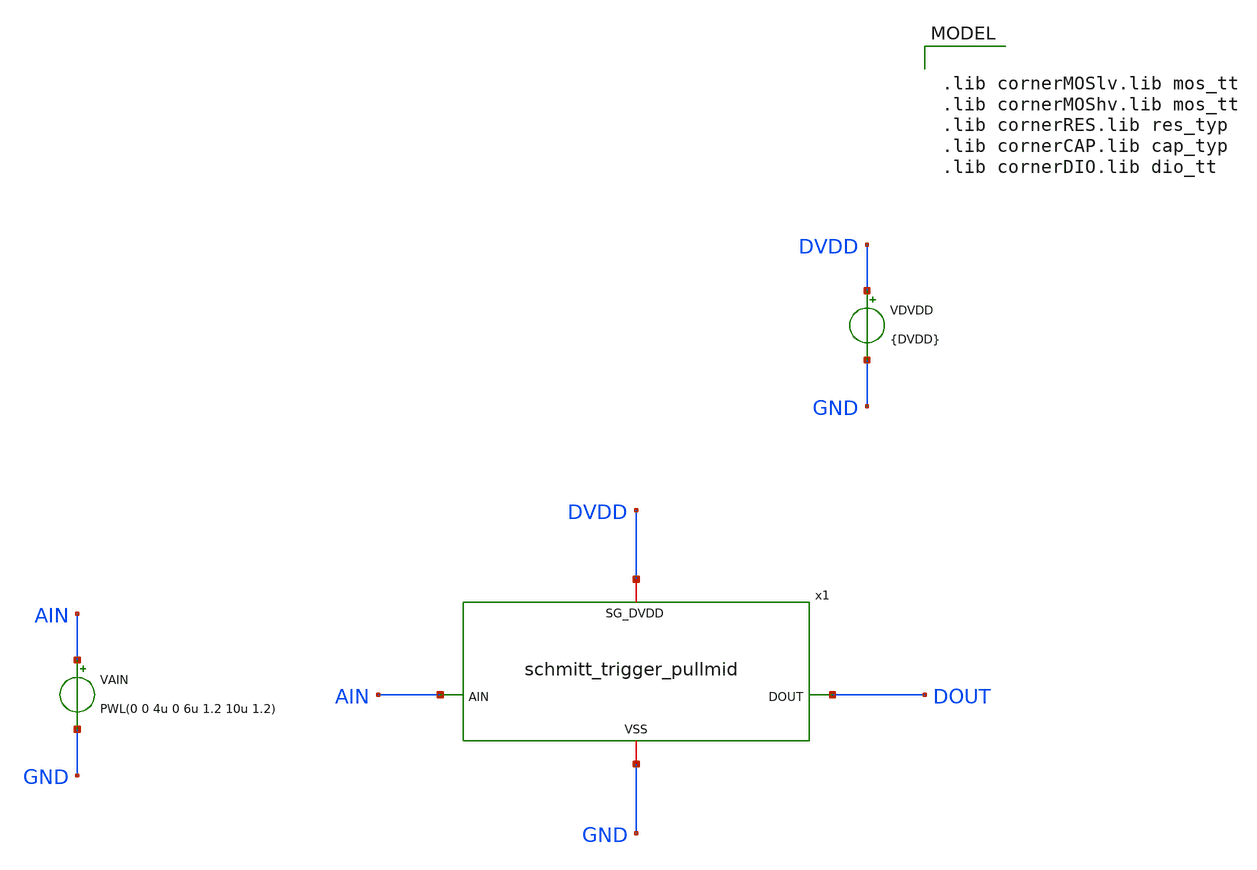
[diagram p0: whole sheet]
** sch_path: macros/schmitt_trigger_pullmid/testbenches/xschem/schmitt_trigger_pullmid_tb_dc.sch
**.subckt schmitt_trigger_pullmid_tb_dc
x1 DVDD AIN DOUT GND schmitt_trigger_pullmid
VAIN AIN GND PWL(0 0 4u 0 6u 1.2 10u 1.2)
VDVDD DVDD GND {DVDD}
**** begin user architecture code


.include ../../../netlist/pex/schmitt_trigger_pullmid_magic_pex_3.spice
.param DVDD=1.2
.csparam DVDD=DVDD
.temp 27
.options savecurrents klu method=gear reltol=1e-3 abstol=1e-12 gmin=1e-12
.control

save all

tran 100p 10u
write @schname\.raw

plot ain dout

unset appendwrite
set wr_vecnames
set wr_singlescale
wrdata ../plot_simulations/data/@schname\.txt v(ain) v(dout)

*quit
.endc



.lib cornerMOSlv.lib mos_tt
.lib cornerMOShv.lib mos_tt
.lib cornerRES.lib res_typ
.lib cornerCAP.lib cap_typ
.lib cornerDIO.lib dio_tt

**** end user architecture code
**.ends

* expanding   symbol:  schmitt_trigger_pullmid.sym # of pins=4
** sym_path: schmitt_trigger_pullmid.sym
** sch_path: schmitt_trigger_pullmid.sch
.subckt schmitt_trigger_pullmid SG_DVDD AIN DOUT VSS
*.iopin SG_DVDD
*.iopin VSS
*.ipin AIN
*.opin DOUT
Vmeas6 AIN net1 0
.save i(vmeas6)
XR1 SG_DVDD MID VSS rhigh w=0.5e-6 l=3.412e-05 m=1 b=0 mm_ok=1
XR2 MID VSS VSS rhigh w=0.5e-6 l=3.412e-05 m=1 b=0 mm_ok=1
XR3 net1 MID VSS rhigh w=0.5e-6 l=2.7172e-04 m=1 b=0 mm_ok=1
XC4 VSS SG_DVDD cap_cmomf w=30.0e-6 l=75.0e-6 mmin=1 mmax=4 subblock=0 rfmodel=0 subscale=1 m=1
+ mm_ok=1
XM4 DOUT net1 DLT VSS sg13_lv_nmos w=1u l=0.3u ng=1 m=1 mm_ok=1
XM5 DHT net1 SG_DVDD SG_DVDD sg13_lv_pmos w=1u l=0.3u ng=1 m=1 mm_ok=1
XM3 DOUT net1 DHT SG_DVDD sg13_lv_pmos w=1u l=0.3u ng=1 m=1 mm_ok=1
XM7 VSS DOUT DHT SG_DVDD sg13_lv_pmos w=1u l=0.3u ng=1 m=1 mm_ok=1
XM6 DLT net1 VSS VSS sg13_lv_nmos w=1u l=0.3u ng=1 m=1 mm_ok=1
XM8 SG_DVDD DOUT DLT VSS sg13_lv_nmos w=1u l=0.3u ng=1 m=1 mm_ok=1
.ends

.end
